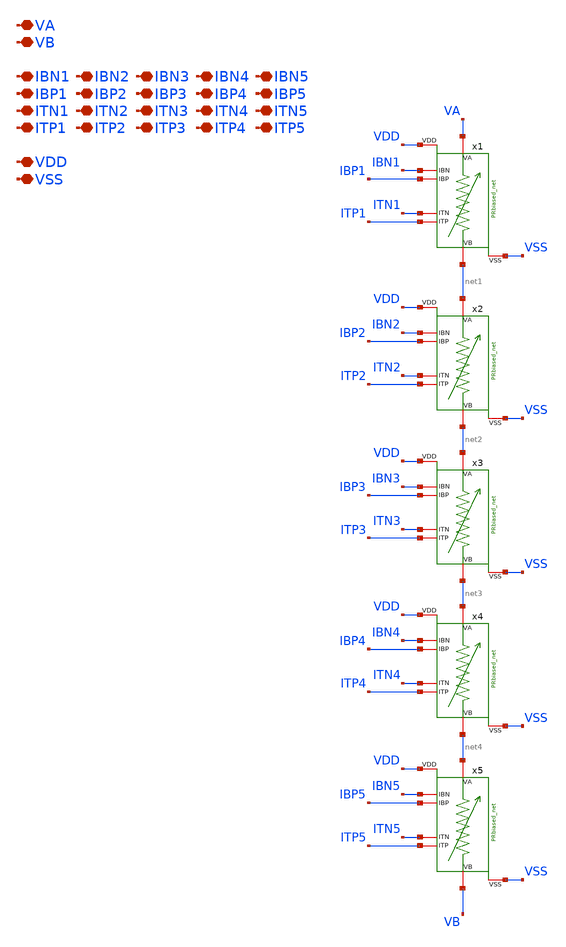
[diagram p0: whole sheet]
** sch_path: TIA_Filter/PseudoResistor/PRbiased_net_x5.sch
**.subckt PRbiased_net_x5 VA VB IBN1 IBP1 ITN1 ITP1 VDD VSS IBN2 IBP2 ITN2 ITP2 IBN3 IBP3 ITN3 ITP3
*+ IBN4 IBP4 ITN4 ITP4 IBN5 IBP5 ITN5 ITP5
*.iopin VA
*.iopin VB
*.iopin IBN1
*.iopin IBP1
*.iopin ITN1
*.iopin ITP1
*.iopin VDD
*.iopin VSS
*.iopin IBN2
*.iopin IBP2
*.iopin ITN2
*.iopin ITP2
*.iopin IBN3
*.iopin IBP3
*.iopin ITN3
*.iopin ITP3
*.iopin IBN4
*.iopin IBP4
*.iopin ITN4
*.iopin ITP4
*.iopin IBN5
*.iopin IBP5
*.iopin ITN5
*.iopin ITP5
x1 VA net1 IBN1 IBP1 ITN1 ITP1 VDD VSS PRbiased_net
x2 net1 net2 IBN2 IBP2 ITN2 ITP2 VDD VSS PRbiased_net
x3 net2 net3 IBN3 IBP3 ITN3 ITP3 VDD VSS PRbiased_net
x4 net3 net4 IBN4 IBP4 ITN4 ITP4 VDD VSS PRbiased_net
x5 net4 VB IBN5 IBP5 ITN5 ITP5 VDD VSS PRbiased_net
**.ends
.end
